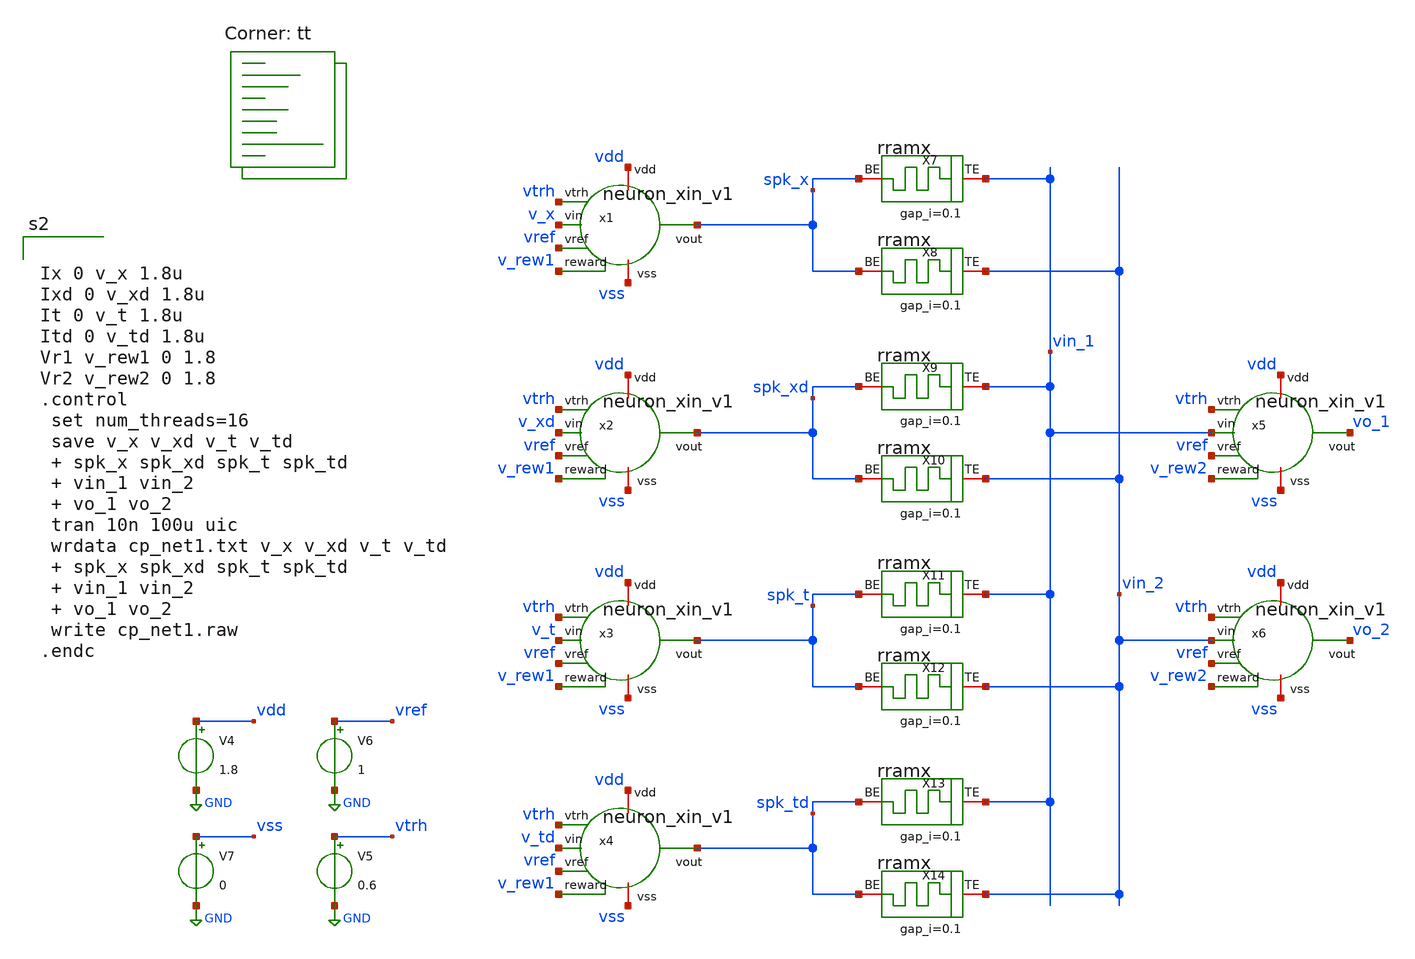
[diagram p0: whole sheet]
** sch_path: tests/cp_net1.sch
**.subckt cp_net1
V4 vdd GND 1.8
V5 vtrh GND 0.6
V6 vref GND 1
V7 vss GND 0
x1 vdd vss spk_x v_x vtrh vref v_rew1 neuron_xin_v1
x2 vdd vss spk_xd v_xd vtrh vref v_rew1 neuron_xin_v1
x3 vdd vss spk_t v_t vtrh vref v_rew1 neuron_xin_v1
x4 vdd vss spk_td v_td vtrh vref v_rew1 neuron_xin_v1
x5 vdd vss vo_1 vin_1 vtrh vref v_rew2 neuron_xin_v1
x6 vdd vss vo_2 vin_2 vtrh vref v_rew2 neuron_xin_v1
X7 vin_1 spk_x rram_cell gap_i=0.1
X8 vin_2 spk_x rram_cell gap_i=0.1
X9 vin_1 spk_xd rram_cell gap_i=0.1
X10 vin_2 spk_xd rram_cell gap_i=0.1
X11 vin_1 spk_t rram_cell gap_i=0.1
X12 vin_2 spk_t rram_cell gap_i=0.1
X13 vin_1 spk_td rram_cell gap_i=0.1
X14 vin_2 spk_td rram_cell gap_i=0.1
**** begin user architecture code


Ix 0 v_x 1.8u
Ixd 0 v_xd 1.8u
It 0 v_t 1.8u
Itd 0 v_td 1.8u
Vr1 v_rew1 0 1.8
Vr2 v_rew2 0 1.8
.control
 set num_threads=16
 save v_x v_xd v_t v_td
 + spk_x spk_xd spk_t spk_td
 + vin_1 vin_2
 + vo_1 vo_2
 tran 10n 100u uic
 wrdata cp_net1.txt v_x v_xd v_t v_td
 + spk_x spk_xd spk_t spk_td
 + vin_1 vin_2
 + vo_1 vo_2
 write cp_net1.raw
.endc



.lib $::SKYWATER_MODELS/sky130.lib.spice tt

.subckt rram_cell BE TE gap_i=0.1
N1 BE TE rram_model
.model rram_model rram gap_initial={gap_i}
.ends rram_cell

.control
pre_osdi /foss/designs/spike_130/designs/prubs/rram.osdi
.endc

**** end user architecture code
**.ends
.GLOBAL GND
.end
